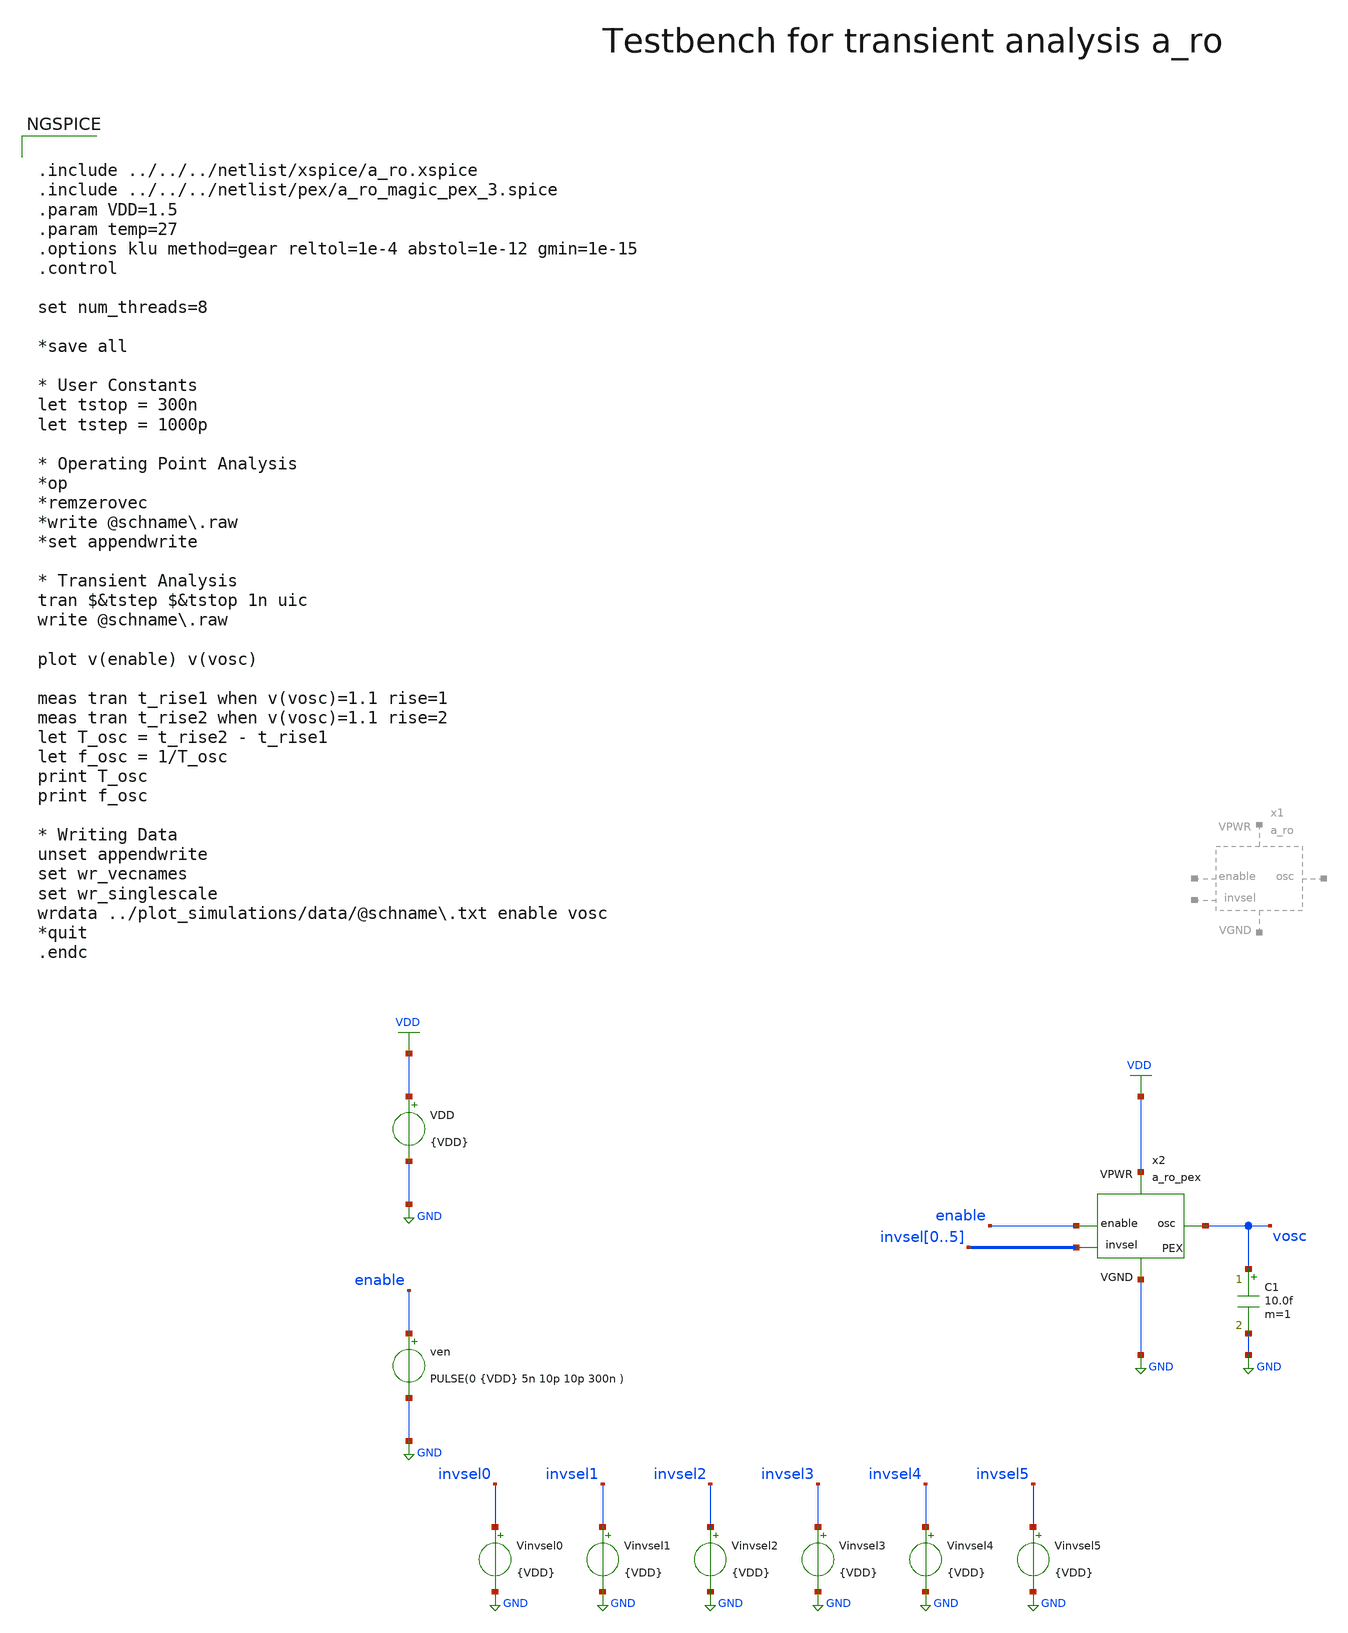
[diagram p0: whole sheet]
** sch_path: macros/heichips26_digital_project/macros/a_ro/testbenches/xschem/a_ro_tb_tran.sch
**.subckt a_ro_tb_tran
VDD VDD GND {VDD}
ven enable GND PULSE(0 {VDD} 5n 10p 10p 300n )
x2 VDD GND enable vosc invsel0 invsel1 invsel2 invsel3 invsel4 invsel5 a_ro_pex
C1 vosc GND 10.0f m=1
Vinvsel0 invsel0 GND {VDD}
Vinvsel1 invsel1 GND {VDD}
Vinvsel2 invsel2 GND {VDD}
Vinvsel3 invsel3 GND {VDD}
Vinvsel4 invsel4 GND {VDD}
Vinvsel5 invsel5 GND {VDD}
**** begin user architecture code


.include ../../../netlist/xspice/a_ro.xspice
.include ../../../netlist/pex/a_ro_magic_pex_3.spice
.param VDD=1.5
.param temp=27
.options klu method=gear reltol=1e-4 abstol=1e-12 gmin=1e-15
.control

set num_threads=8

*save all

* User Constants
let tstop = 300n
let tstep = 1000p

* Operating Point Analysis
*op
*remzerovec
*write @schname\.raw
*set appendwrite

* Transient Analysis
tran $&tstep $&tstop 1n uic
write @schname\.raw

plot v(enable) v(vosc)

meas tran t_rise1 when v(vosc)=1.1 rise=1
meas tran t_rise2 when v(vosc)=1.1 rise=2
let T_osc = t_rise2 - t_rise1
let f_osc = 1/T_osc
print T_osc
print f_osc

* Writing Data
unset appendwrite
set wr_vecnames
set wr_singlescale
wrdata ../plot_simulations/data/@schname\.txt enable vosc
*quit
.endc


.lib cornerMOSlv.lib mos_tt
.lib cornerMOShv.lib mos_tt
.lib cornerRES.lib res_typ
.lib cornerDIO.lib dio_tt

**** end user architecture code
**.ends
.GLOBAL GND
.GLOBAL VDD
.end
